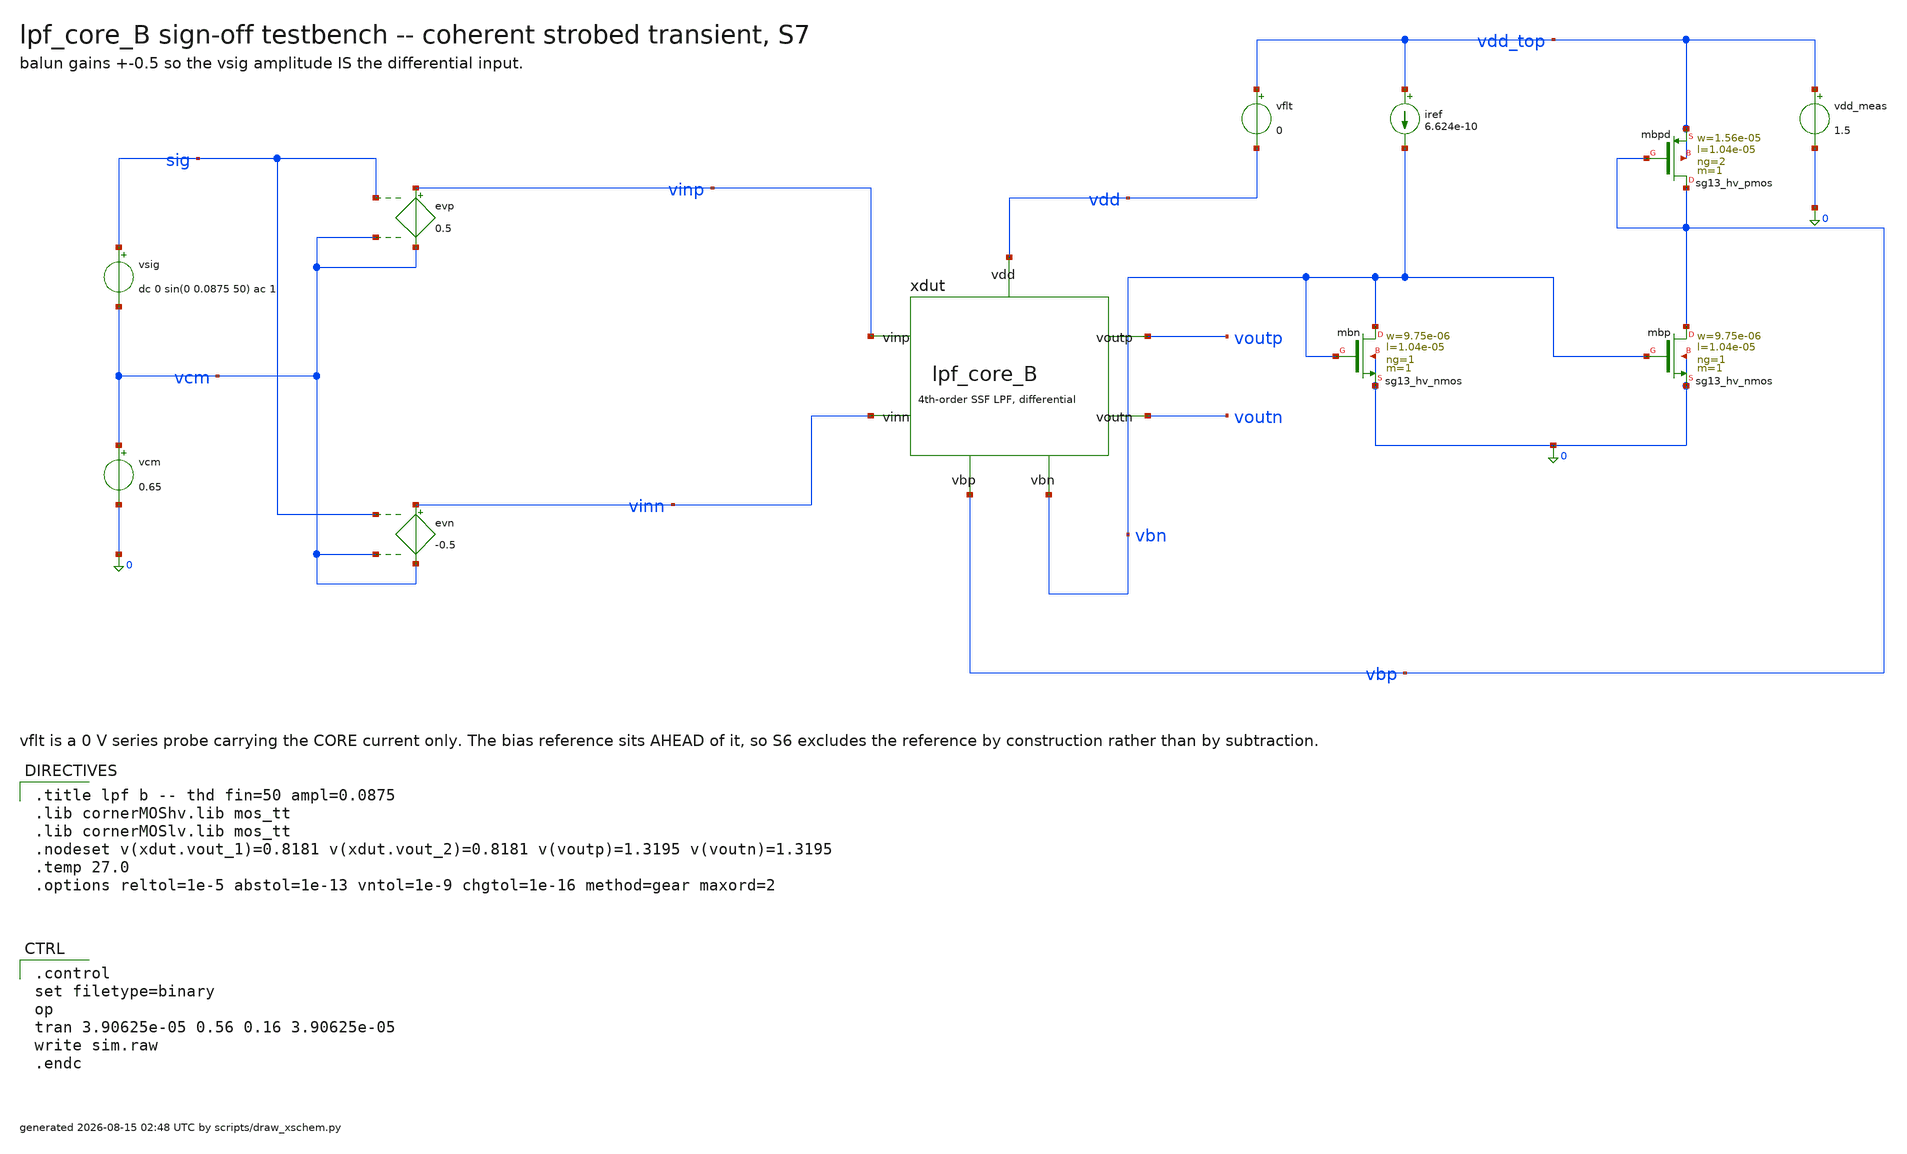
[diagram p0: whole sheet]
** sch_path: signoff/pre-pvt/B-balanced/lpf_tb_B_thd.sch
**.subckt lpf_tb_B_thd
vsig sig vcm dc 0 sin(0 0.0875 50) ac 1
vcm vcm 0 0.65
evp vinp vcm sig vcm 0.5
evn vinn vcm sig vcm -0.5
xdut vinp vinn voutp voutn vbn vbp vdd lpf_core_B
vflt vdd_top vdd 0
vdd_meas vdd_top 0 1.5
iref vdd_top vbn 6.624e-10
Xmbn vbn vbn 0 0 sg13_hv_nmos w=9.75e-06 l=1.04e-05 ng=1 m=1 mm_ok=1
Xmbp vbp vbn 0 0 sg13_hv_nmos w=9.75e-06 l=1.04e-05 ng=1 m=1 mm_ok=1
Xmbpd vbp vbp vdd_top vdd_top sg13_hv_pmos w=1.56e-05 l=1.04e-05 ng=2 m=1 mm_ok=1
**** begin user architecture code

.title lpf b -- thd fin=50 ampl=0.0875
.lib cornerMOShv.lib mos_tt
.lib cornerMOSlv.lib mos_tt
.nodeset v(xdut.vout_1)=0.8181 v(xdut.vout_2)=0.8181 v(voutp)=1.3195 v(voutn)=1.3195
.temp 27.0
.options reltol=1e-5 abstol=1e-13 vntol=1e-9 chgtol=1e-16 method=gear maxord=2


.control
set filetype=binary
op
tran 3.90625e-05 0.56 0.16 3.90625e-05
write sim.raw
.endc

**** end user architecture code
**.ends

* expanding   symbol:  lpf_core_B.sym # of pins=7
** sym_path: signoff/B-balanced/lpf_core_B.sym
** sch_path: signoff/B-balanced/lpf_core_B.sch
.subckt lpf_core_B vinp vinn voutp voutn vbn vbp vdd
*.ipin vinp
*.ipin vinn
*.opin voutp
*.opin voutn
*.ipin vdd
*.ipin vbn
*.ipin vbp
Xm2 net2 vinp vout_1 vout_1 sg13_lv_pmos w=1.56e-05 l=1.04e-05 ng=2 m=1 mm_ok=1
Xm5 net3 vinn vout_2 vout_2 sg13_lv_pmos w=1.56e-05 l=1.04e-05 ng=2 m=1 mm_ok=1
Xm4 vout_1 net2 0 0 sg13_hv_nmos w=7.8e-06 l=5.2e-06 ng=1 m=1 mm_ok=1
Xm8 vout_2 net3 0 0 sg13_hv_nmos w=7.8e-06 l=5.2e-06 ng=1 m=1 mm_ok=1
Xm9 net2 vbn 0 0 sg13_hv_nmos w=9.75e-06 l=1.04e-05 ng=1 m=1 mm_ok=1
Xm10 net3 vbn 0 0 sg13_hv_nmos w=9.75e-06 l=1.04e-05 ng=1 m=1 mm_ok=1
Xmst vout_1 vbn net4 net4 sg13_hv_pmos w=1.62e-06 l=1.092e-05 ng=1 m=1 mm_ok=1
Xmstn vout_2 vbn net1 net1 sg13_hv_pmos w=1.62e-06 l=1.092e-05 ng=1 m=1 mm_ok=1
Xm0 net4 vout_1 voutp voutp sg13_hv_pmos w=1.56e-05 l=1.04e-05 ng=2 m=1 mm_ok=1
Xm1 net1 vout_2 voutn voutn sg13_hv_pmos w=1.56e-05 l=1.04e-05 ng=2 m=1 mm_ok=1
Xm14 voutp net4 vdd vdd sg13_hv_pmos w=8.085e-06 l=1.56e-05 ng=1 m=1 mm_ok=1
Xm15 voutn net1 vdd vdd sg13_hv_pmos w=8.085e-06 l=1.56e-05 ng=1 m=1 mm_ok=1
c13 net2 vout_1 6.525e-12 m=1
c17 net3 vout_2 6.525e-12 m=1
c19 vout_2 vout_1 2.40639e-11 m=1
c1 voutp net4 4.84072e-11 m=1
c10 voutn net1 4.84072e-11 m=1
c12 voutn voutp 1.89263e-11 m=1
.ends

.end
